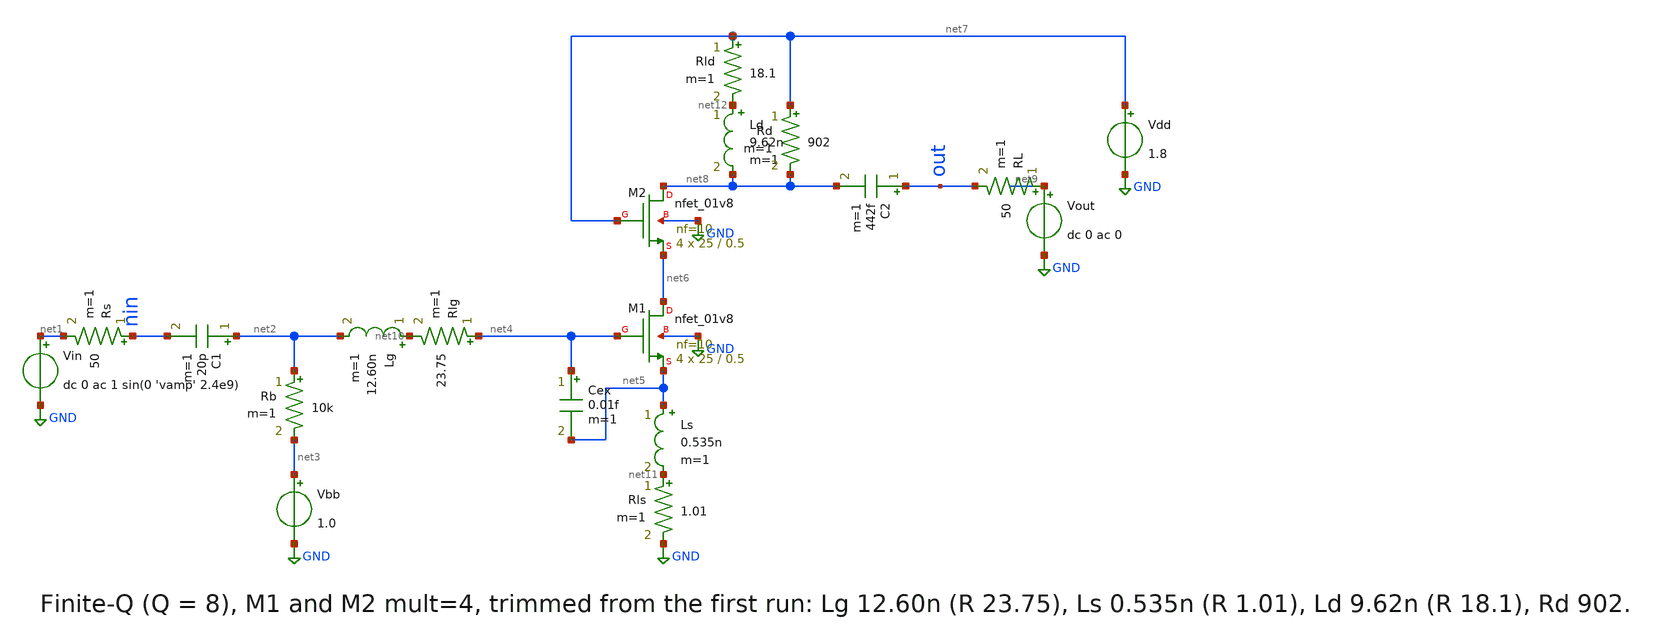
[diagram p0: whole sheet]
** sch_path: 03-sky130-lna-2p4ghz/schematic/lna_q8_m4.sch
**.subckt lna_q8_m4
XM1 net6 net4 net5 GND sky130_fd_pr__nfet_01v8 L=0.5 W=25 nf=10 ad='int((nf+1)/2) * W/nf * 0.29' as='int((nf+2)/2) * W/nf * 0.29'
+ pd='2*int((nf+1)/2) * (W/nf + 0.29)' ps='2*int((nf+2)/2) * (W/nf + 0.29)' nrd='0.29 / W' nrs='0.29 / W'
+ sa=0 sb=0 sd=0 mult=4 m=4
XM2 net8 net7 net6 GND sky130_fd_pr__nfet_01v8 L=0.5 W=25 nf=10 ad='int((nf+1)/2) * W/nf * 0.29' as='int((nf+2)/2) * W/nf * 0.29'
+ pd='2*int((nf+1)/2) * (W/nf + 0.29)' ps='2*int((nf+2)/2) * (W/nf + 0.29)' nrd='0.29 / W' nrs='0.29 / W'
+ sa=0 sb=0 sd=0 mult=4 m=4
Vin net1 GND dc 0 ac 1 sin(0 'vamp' 2.4e9)
Rs nin net1 50 m=1
C1 net2 nin 20p m=1
Lg net10 net2 12.60n m=1
Rlg net4 net10 23.75 m=1
Rb net2 net3 10k m=1
Vbb net3 GND 1.0
Cex net4 net5 0.01f m=1
Ls net5 net11 0.535n m=1
Rls net11 GND 1.01 m=1
Ld net12 net8 9.62n m=1
Rld net7 net12 18.1 m=1
Rd net7 net8 902 m=1
C2 out net8 442f m=1
RL net9 out 50 m=1
Vout net9 GND dc 0 ac 0
Vdd net7 GND 1.8
**** begin user architecture code


.lib /home/nehan/.volare/sky130A/libs.tech/ngspice/sky130.lib.spice tt
.GLOBAL GND
.param vamp=0.001
.control
save all

op
print v(nin) v(out) -i(Vdd)

* ---- S-parameters, 2.0 to 2.8 GHz, 1 MHz steps ----
alter vin acmag = 1
alter vout acmag = 0
ac lin 3001 1e9 4e9
let s11 = 2*v(nin)-1
let s21 = 2*v(out)

alter vin acmag = 0
alter vout acmag = 1
ac lin 3001 1e9 4e9
let s22 = 2*v(out)-1
let s12 = 2*v(nin)
let s11 = ac1.s11*1
let s21 = ac1.s21*1
let s11db = db(s11)
let s21db = db(s21)
let s22db = db(s22)
let zin = 50*(1+s11)/(1-s11)
let rin = real(zin)
let xin = imag(zin)
let zout = 50*(1+s22)/(1-s22)
let rout = real(zout)
let xout = imag(zout)
let s12db = db(s12)
let dlt = s11*s22 - s12*s21
let dmag = mag(dlt)
let kfac = (1 - mag(s11)*mag(s11) - mag(s22)*mag(s22) + dmag*dmag)/(2*mag(s12*s21))
let mu = (1 - mag(s11)*mag(s11))/(mag(s22 - dlt*conj(s11)) + mag(s12*s21))
let mup = (1 - mag(s22)*mag(s22))/(mag(s11 - dlt*conj(s22)) + mag(s12*s21))

* ---- Export S-parameters, impedances and stability ----
set wr_singlescale
set wr_vecnames
wrdata results/data/q8_m4_sparams.dat s11db s21db s12db s22db rin xin rout xout kfac dmag mu mup

plot s11db s22db vs frequency title 'S11 and S22 (dB)'
plot s21db vs frequency title 'S21 (dB)'

meas ac s11_2p4G find s11db at=2.4e9
meas ac s21_2p4G find s21db at=2.4e9
meas ac s22_2p4G find s22db at=2.4e9
meas ac rin_2p4G find rin at=2.4e9
meas ac xin_2p4G find xin at=2.4e9
meas ac rout_2p4G find rout at=2.4e9
meas ac xout_2p4G find xout at=2.4e9
meas ac s12_2p4G find s12db at=2.4e9
meas ac k_2p4G find kfac at=2.4e9
meas ac mu_2p4G find mu at=2.4e9
meas ac mup_2p4G find mup at=2.4e9
meas ac f_s11best min_at s11db

* ---- bandwidth ----
meas ac f11_lo when s11db=-10 cross=1
meas ac f11_hi when s11db=-10 cross=2
meas ac f22_lo when s22db=-10 cross=1
meas ac f22_hi when s22db=-10 cross=2
let s21n = s21db - vecmax(s21db)
meas ac f3_lo when s21n=-3 cross=1
meas ac f3_hi when s21n=-3 cross=2

* ---- P1dB, IIP3 and OIP3 estimates: input power sweep at 2.4 GHz ----
set g0 = $&s21_2p4g

* ---- noise figure at 2.4 GHz (Rs = 50 ohm at the input) ----
alter vin acmag = 1
alter vout acmag = 0
noise v(out) vin lin 41 1e9 5e9
setplot noise2
let nf = 10*log10(inoise_spectrum*inoise_spectrum/(4*1.380649e-23*300.15*50))
wrdata results/data/q8_m4_nf.dat nf
plot nf vs frequency title 'Noise figure (dB)'
let f24 = frequency[14]
print f24 nf[14]
foreach pdbm -50 -30 -20 -18 -16 -15 -14 -13 -12 -11 -10 -9 -8 -6
  let amp = sqrt(8*50*1e-3*10^($pdbm/10))
  alterparam vamp = $&amp
  reset
  tran 10p 20n 0 10p
  let amp = sqrt(8*50*1e-3*10^($pdbm/10))
  let cf = v(out)*cos(2*pi*2.4e9*time)
  let sf = v(out)*sin(2*pi*2.4e9*time)
  meas tran mcf integ cf from=14n to=16.916667n
  meas tran msf integ sf from=14n to=16.916667n
  meas tran idd avg i(vdd) from=14n to=16.916667n
  let vf = 2/2.916667e-9*sqrt(mcf*mcf+msf*msf)
  let poutf = 10*log10(vf*vf/100/1e-3)
  let gf = 20*log10(2*vf/amp)
  let dg = gf - $g0
  let cmp = 10^(dg/20)
  let iip3 = $pdbm + 10*log10(1/(1-cmp))
  let oip3 = iip3 + $g0
  let pdc = -idd*1.8
  let eff = vf*vf/100/pdc
  echo Pin = $pdbm dBm  Pout = $&poutf dBm  Gain = $&gf dB  Change = $&dg dB  IIP3est = $&iip3 dBm
+  OIP3est = $&oip3 dBm  Pdc = $&pdc W  Eff = $&eff
end
.endc


**** end user architecture code
**.ends
.GLOBAL GND
.end
